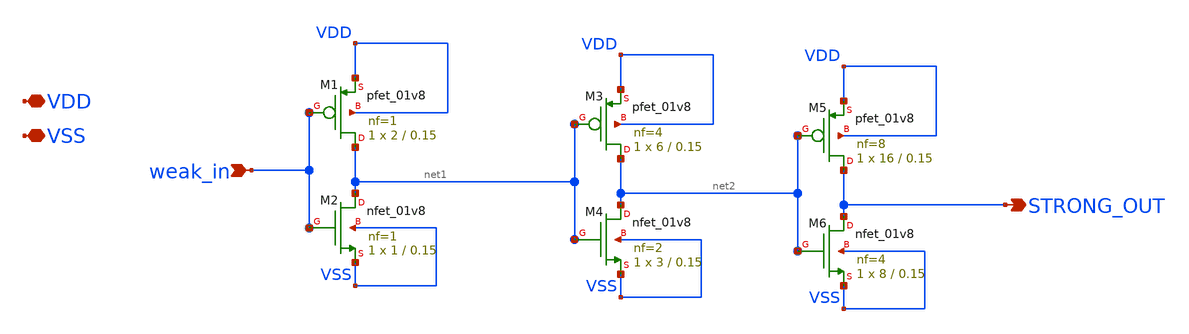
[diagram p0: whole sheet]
** sch_path: xschem/inverter_chain.sch
**.subckt inverter_chain VDD VSS weak_in STRONG_OUT
*.iopin VDD
*.iopin VSS
*.ipin weak_in
*.opin STRONG_OUT
XM1 net1 weak_in VDD VDD sky130_fd_pr__pfet_01v8 L=0.15 W=2 nf=1 ad='int((nf+1)/2) * W/nf * 0.29' as='int((nf+2)/2) * W/nf * 0.29'
+ pd='2*int((nf+1)/2) * (W/nf + 0.29)' ps='2*int((nf+2)/2) * (W/nf + 0.29)' nrd='0.29 / W' nrs='0.29 / W'
+ sa=0 sb=0 sd=0 mult=1 m=1
XM2 net1 weak_in VSS VSS sky130_fd_pr__nfet_01v8 L=0.15 W=1 nf=1 ad='int((nf+1)/2) * W/nf * 0.29' as='int((nf+2)/2) * W/nf * 0.29'
+ pd='2*int((nf+1)/2) * (W/nf + 0.29)' ps='2*int((nf+2)/2) * (W/nf + 0.29)' nrd='0.29 / W' nrs='0.29 / W'
+ sa=0 sb=0 sd=0 mult=1 m=1
XM3 net2 net1 VDD VDD sky130_fd_pr__pfet_01v8 L=0.15 W=6 nf=4 ad='int((nf+1)/2) * W/nf * 0.29' as='int((nf+2)/2) * W/nf * 0.29'
+ pd='2*int((nf+1)/2) * (W/nf + 0.29)' ps='2*int((nf+2)/2) * (W/nf + 0.29)' nrd='0.29 / W' nrs='0.29 / W'
+ sa=0 sb=0 sd=0 mult=1 m=1
XM4 net2 net1 VSS VSS sky130_fd_pr__nfet_01v8 L=0.15 W=3 nf=2 ad='int((nf+1)/2) * W/nf * 0.29' as='int((nf+2)/2) * W/nf * 0.29'
+ pd='2*int((nf+1)/2) * (W/nf + 0.29)' ps='2*int((nf+2)/2) * (W/nf + 0.29)' nrd='0.29 / W' nrs='0.29 / W'
+ sa=0 sb=0 sd=0 mult=1 m=1
XM5 STRONG_OUT net2 VDD VDD sky130_fd_pr__pfet_01v8 L=0.15 W=16 nf=8 ad='int((nf+1)/2) * W/nf * 0.29'
+ as='int((nf+2)/2) * W/nf * 0.29' pd='2*int((nf+1)/2) * (W/nf + 0.29)' ps='2*int((nf+2)/2) * (W/nf + 0.29)'
+ nrd='0.29 / W' nrs='0.29 / W' sa=0 sb=0 sd=0 mult=1 m=1
XM6 STRONG_OUT net2 VSS VSS sky130_fd_pr__nfet_01v8 L=0.15 W=8 nf=4 ad='int((nf+1)/2) * W/nf * 0.29'
+ as='int((nf+2)/2) * W/nf * 0.29' pd='2*int((nf+1)/2) * (W/nf + 0.29)' ps='2*int((nf+2)/2) * (W/nf + 0.29)'
+ nrd='0.29 / W' nrs='0.29 / W' sa=0 sb=0 sd=0 mult=1 m=1
**.ends
.end
